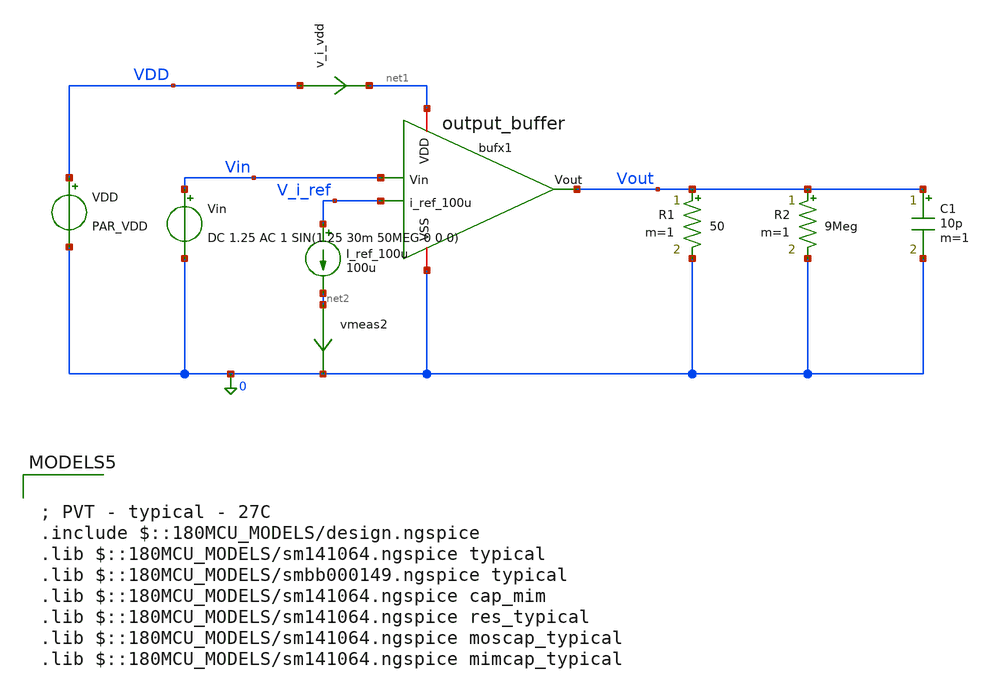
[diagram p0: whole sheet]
** sch_path: designs/output_buffer/testbench/tb_output_buffer_nfet_input.sch
**.subckt tb_output_buffer_nfet_input
x1 Vout Vin V_i_ref net1 0 output_buffer
I_ref_100u V_i_ref net2 100u
Vin Vin 0 DC 1.25 AC 1 SIN(1.25 30m 50MEG 0 0 0)
VDD VDD 0 PAR_VDD
R1 Vout 0 50 m=1
vmeas2 net2 0 0
.save i(vmeas2)
R2 Vout 0 9Meg m=1
C1 Vout 0 10p m=1
v_i_vdd VDD net1 0
.save i(v_i_vdd)
**** begin user architecture code

; PVT - typical - 27C
.include $::180MCU_MODELS/design.ngspice
.lib $::180MCU_MODELS/sm141064.ngspice typical
.lib $::180MCU_MODELS/smbb000149.ngspice typical
.lib $::180MCU_MODELS/sm141064.ngspice cap_mim
.lib $::180MCU_MODELS/sm141064.ngspice res_typical
.lib $::180MCU_MODELS/sm141064.ngspice moscap_typical
.lib $::180MCU_MODELS/sm141064.ngspice mimcap_typical



** PARAMS

.PARAM PAR_VDD=3.27

.control
destroy all
save all
save @m.x1.xm1.m0[gm]
save @m.x1.xm2.m0[gm]
save @m.x1.xm2.m0[gds]
save @m.x1.xm5.m0[gds]

write tb_output_buffer.raw
op

print i(v_i_vdd)
dc Vin 0.1 3.3 0.01
let gain_slope = deriv(vout)

plot Vin Vout ; input, output
plot Vout vs Vin gain_slope vs vin; output vs input and slope of gain
plot vdb(gain_slope) vs vin; gain slope in db
plot i(v_i_vdd) i(vmeas2) i(v.x1.vmeas1) i(v.x1.vmeas2) i(v.x1.vmeas3); internal current biases

plot @m.x1.xm1.m0[gm] @m.x1.xm2.m0[gm]
;plot 1/@m.x1.xm2.m0[gds] 1/@m.x1.xm5.m0[gds]

ac dec 100 1 10G
let gain = vout/vin
let gain_db = db(gain)
plot gain_db

tran 0.1n 10u
plot vin vout
linearize vin vout
fft vin vout
plot db(vin) vs frequency db(vout) vs frequency xlimit 0 120MEG


;parametric sweep for compensation capacitor

;setplot const
;let start_c = 100f
;let stop_c = 3p
;let delta_c = 300f
;let current_c = start_c

;while current_c le stop_c
;	print current_c
;	alter c.x1.c2 = current_c
;	ac dec 100 1 10G
;	let gain = vout/vin;
;	let gain_db = db(gain)
;
;	let current_c = current_c + delta_c
;end
;plot  ac2.gain_db ac3.gain_db ac4.gain_db ac5.gain_db ac6.gain_db ac7.gain_db ac8.gain_db
+ ac9.gain_db ac10.gain_db ac11.gain_db
.endc


**** end user architecture code
**.ends

* expanding   symbol:  output_buffer/schematic/output_buffer.sym # of pins=5
** sym_path: designs/output_buffer/schematic/output_buffer.sym
** sch_path: designs/output_buffer/schematic/output_buffer.sch
.subckt output_buffer Vout Vin i_ref_100u VDD VSS
*.ipin Vin
*.opin Vout
*.ipin i_ref_100u
*.iopin VDD
*.iopin VSS
XM1 net1 Vin net2 VSS nfet_03v3 L=0.28u W=80u nf=8 ad='int((nf+1)/2) * W/nf * 0.18u' as='int((nf+2)/2) * W/nf * 0.18u'
+ pd='2*int((nf+1)/2) * (W/nf + 0.18u)' ps='2*int((nf+2)/2) * (W/nf + 0.18u)' nrd='0.18u / W' nrs='0.18u / W'
+ sa=0 sb=0 sd=0 m=1
XM2 net5 net1 VDD VDD pfet_03v3 L=0.28u W=25u nf=10 ad='int((nf+1)/2) * W/nf * 0.18u' as='int((nf+2)/2) * W/nf * 0.18u'
+ pd='2*int((nf+1)/2) * (W/nf + 0.18u)' ps='2*int((nf+2)/2) * (W/nf + 0.18u)' nrd='0.18u / W' nrs='0.18u / W'
+ sa=0 sb=0 sd=0 m=1
XM3 net1 i_ref_100u VDD VDD pfet_03v3 L=1u W=20u nf=1 ad='int((nf+1)/2) * W/nf * 0.18u' as='int((nf+2)/2) * W/nf * 0.18u'
+ pd='2*int((nf+1)/2) * (W/nf + 0.18u)' ps='2*int((nf+2)/2) * (W/nf + 0.18u)' nrd='0.18u / W' nrs='0.18u / W'
+ sa=0 sb=0 sd=0 m=1
XM4 i_ref_100u i_ref_100u VDD VDD pfet_03v3 L=1u W=1u nf=1 ad='int((nf+1)/2) * W/nf * 0.18u' as='int((nf+2)/2) * W/nf * 0.18u'
+ pd='2*int((nf+1)/2) * (W/nf + 0.18u)' ps='2*int((nf+2)/2) * (W/nf + 0.18u)' nrd='0.18u / W' nrs='0.18u / W'
+ sa=0 sb=0 sd=0 m=1
XM5 net6 net3 VSS VSS nfet_03v3 L=1u W=40u nf=1 ad='int((nf+1)/2) * W/nf * 0.18u' as='int((nf+2)/2) * W/nf * 0.18u'
+ pd='2*int((nf+1)/2) * (W/nf + 0.18u)' ps='2*int((nf+2)/2) * (W/nf + 0.18u)' nrd='0.18u / W' nrs='0.18u / W'
+ sa=0 sb=0 sd=0 m=1
R1 net4 net3 10G m=1
vmeas2 net5 Vout 0
.save i(vmeas2)
Vmeas1 Vout net6 0
.save i(vmeas1)
C1 net1 net3 10p m=1
XM6 net4 i_ref_100u VDD VDD pfet_03v3 L=1u W=1u nf=1 ad='int((nf+1)/2) * W/nf * 0.18u' as='int((nf+2)/2) * W/nf * 0.18u'
+ pd='2*int((nf+1)/2) * (W/nf + 0.18u)' ps='2*int((nf+2)/2) * (W/nf + 0.18u)' nrd='0.18u / W' nrs='0.18u / W'
+ sa=0 sb=0 sd=0 m=1
XM7 net4 net4 VSS VSS nfet_03v3 L=1u W=1u nf=1 ad='int((nf+1)/2) * W/nf * 0.18u' as='int((nf+2)/2) * W/nf * 0.18u'
+ pd='2*int((nf+1)/2) * (W/nf + 0.18u)' ps='2*int((nf+2)/2) * (W/nf + 0.18u)' nrd='0.18u / W' nrs='0.18u / W'
+ sa=0 sb=0 sd=0 m=1
Vmeas3 net2 Vout 0
.save i(vmeas3)
.ends

.end
